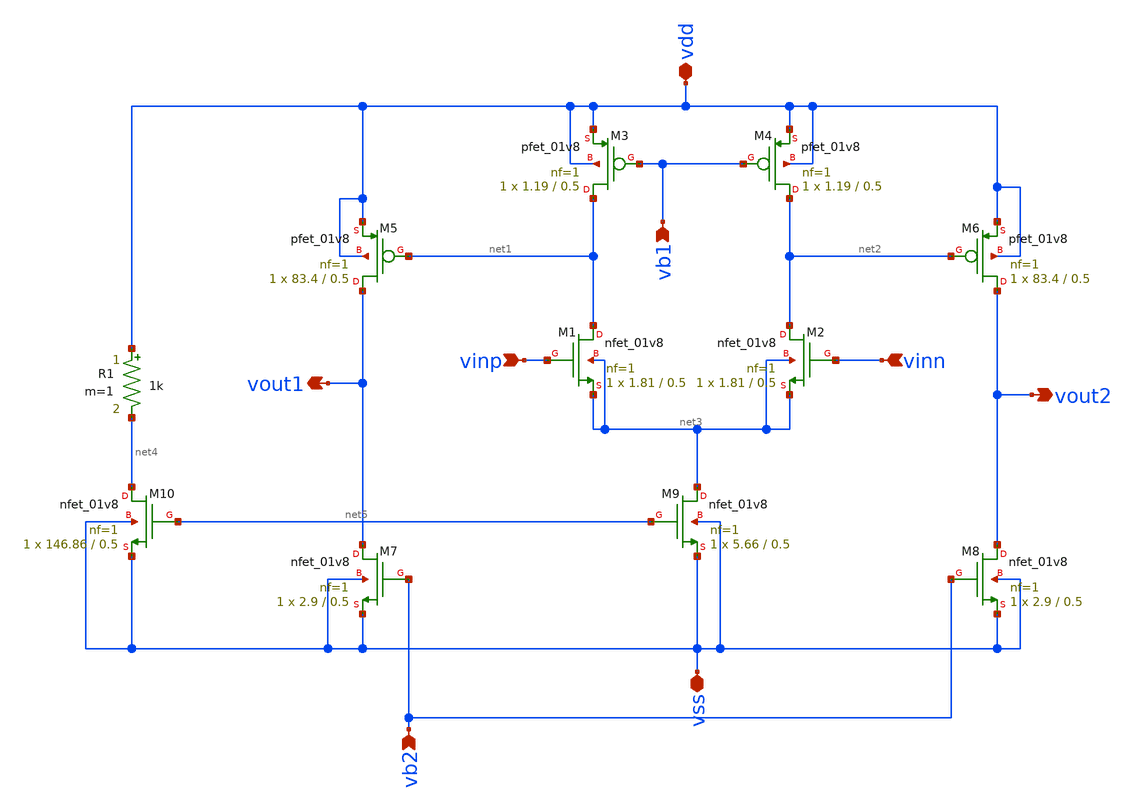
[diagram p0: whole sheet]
** sch_path: sch/opamp_two_stage.sch
**.subckt opamp_two_stage vinp vinn vout2 vout1 vss vb2 vb1 vdd
*.ipin vinp
*.ipin vinn
*.opin vout2
*.opin vout1
*.iopin vss
*.ipin vb2
*.ipin vb1
*.iopin vdd
XM1 net1 vinp net3 net3 sky130_fd_pr__nfet_01v8 L=0.5 W=1.81 nf=1 ad='int((nf+1)/2) * W/nf * 0.29' as='int((nf+2)/2) * W/nf * 0.29'
+ pd='2*int((nf+1)/2) * (W/nf + 0.29)' ps='2*int((nf+2)/2) * (W/nf + 0.29)' nrd='0.29 / W' nrs='0.29 / W'
+ sa=0 sb=0 sd=0 mult=1 m=1
XM2 net2 vinn net3 net3 sky130_fd_pr__nfet_01v8 L=0.5 W=1.81 nf=1 ad='int((nf+1)/2) * W/nf * 0.29' as='int((nf+2)/2) * W/nf * 0.29'
+ pd='2*int((nf+1)/2) * (W/nf + 0.29)' ps='2*int((nf+2)/2) * (W/nf + 0.29)' nrd='0.29 / W' nrs='0.29 / W'
+ sa=0 sb=0 sd=0 mult=1 m=1
XM3 net1 vb1 vdd vdd sky130_fd_pr__pfet_01v8 L=0.5 W=1.19 nf=1 ad='int((nf+1)/2) * W/nf * 0.29' as='int((nf+2)/2) * W/nf * 0.29'
+ pd='2*int((nf+1)/2) * (W/nf + 0.29)' ps='2*int((nf+2)/2) * (W/nf + 0.29)' nrd='0.29 / W' nrs='0.29 / W'
+ sa=0 sb=0 sd=0 mult=1 m=1
XM4 net2 vb1 vdd vdd sky130_fd_pr__pfet_01v8 L=0.5 W=1.19 nf=1 ad='int((nf+1)/2) * W/nf * 0.29' as='int((nf+2)/2) * W/nf * 0.29'
+ pd='2*int((nf+1)/2) * (W/nf + 0.29)' ps='2*int((nf+2)/2) * (W/nf + 0.29)' nrd='0.29 / W' nrs='0.29 / W'
+ sa=0 sb=0 sd=0 mult=1 m=1
XM5 vout1 net1 vdd vdd sky130_fd_pr__pfet_01v8 L=0.5 W=83.4 nf=1 ad='int((nf+1)/2) * W/nf * 0.29' as='int((nf+2)/2) * W/nf * 0.29'
+ pd='2*int((nf+1)/2) * (W/nf + 0.29)' ps='2*int((nf+2)/2) * (W/nf + 0.29)' nrd='0.29 / W' nrs='0.29 / W'
+ sa=0 sb=0 sd=0 mult=1 m=1
XM6 vout2 net2 vdd vdd sky130_fd_pr__pfet_01v8 L=0.5 W=83.4 nf=1 ad='int((nf+1)/2) * W/nf * 0.29' as='int((nf+2)/2) * W/nf * 0.29'
+ pd='2*int((nf+1)/2) * (W/nf + 0.29)' ps='2*int((nf+2)/2) * (W/nf + 0.29)' nrd='0.29 / W' nrs='0.29 / W'
+ sa=0 sb=0 sd=0 mult=1 m=1
XM7 vout1 vb2 vss vss sky130_fd_pr__nfet_01v8 L=0.5 W=2.9 nf=1 ad='int((nf+1)/2) * W/nf * 0.29' as='int((nf+2)/2) * W/nf * 0.29'
+ pd='2*int((nf+1)/2) * (W/nf + 0.29)' ps='2*int((nf+2)/2) * (W/nf + 0.29)' nrd='0.29 / W' nrs='0.29 / W'
+ sa=0 sb=0 sd=0 mult=1 m=1
XM8 vout2 vb2 vss vss sky130_fd_pr__nfet_01v8 L=0.5 W=2.9 nf=1 ad='int((nf+1)/2) * W/nf * 0.29' as='int((nf+2)/2) * W/nf * 0.29'
+ pd='2*int((nf+1)/2) * (W/nf + 0.29)' ps='2*int((nf+2)/2) * (W/nf + 0.29)' nrd='0.29 / W' nrs='0.29 / W'
+ sa=0 sb=0 sd=0 mult=1 m=1
XM9 net3 net5 vss vss sky130_fd_pr__nfet_01v8 L=0.5 W=5.66 nf=1 ad='int((nf+1)/2) * W/nf * 0.29' as='int((nf+2)/2) * W/nf * 0.29'
+ pd='2*int((nf+1)/2) * (W/nf + 0.29)' ps='2*int((nf+2)/2) * (W/nf + 0.29)' nrd='0.29 / W' nrs='0.29 / W'
+ sa=0 sb=0 sd=0 mult=1 m=1
XM10 net4 net5 vss vss sky130_fd_pr__nfet_01v8 L=0.5 W=146.86 nf=1 ad='int((nf+1)/2) * W/nf * 0.29' as='int((nf+2)/2) * W/nf * 0.29'
+ pd='2*int((nf+1)/2) * (W/nf + 0.29)' ps='2*int((nf+2)/2) * (W/nf + 0.29)' nrd='0.29 / W' nrs='0.29 / W'
+ sa=0 sb=0 sd=0 mult=1 m=1
R1 vdd net4 1k m=1
**.ends
.end
